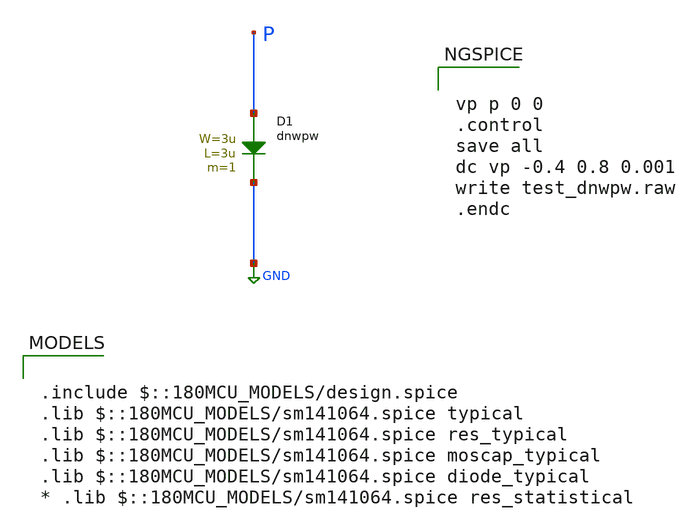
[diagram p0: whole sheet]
** sch_path: cells/xschem/tests/test_dnwpw.sch
* Copyright 2022 GlobalFoundries PDK Authors
* Licensed under the Apache License, Version 2.0 (the "License");
* you may not use this file except in compliance with the License.
* You may obtain a copy of the License at
* https://www.apache.org/licenses/LICENSE-2.0
* Unless required by applicable law or agreed to in writing, software
* distributed under the License is distributed on an "AS IS" BASIS,
* WITHOUT WARRANTIES OR CONDITIONS OF ANY KIND, either express or implied.
* See the License for the specific language governing permissions and
* limitations under the License.
**.subckt test_dnwpw
D1 P GND dnwpw area='3u * 3u ' pj='2*3u + 2*3u ' m=1
**** begin user architecture code

.include $::180MCU_MODELS/design.spice
.lib $::180MCU_MODELS/sm141064.spice typical
.lib $::180MCU_MODELS/sm141064.spice res_typical
.lib $::180MCU_MODELS/sm141064.spice moscap_typical
.lib $::180MCU_MODELS/sm141064.spice diode_typical
* .lib $::180MCU_MODELS/sm141064.spice res_statistical



vp p 0 0
.control
save all
dc vp -0.4 0.8 0.001
write test_dnwpw.raw
.endc


**** end user architecture code
**.ends
.GLOBAL GND
.end
